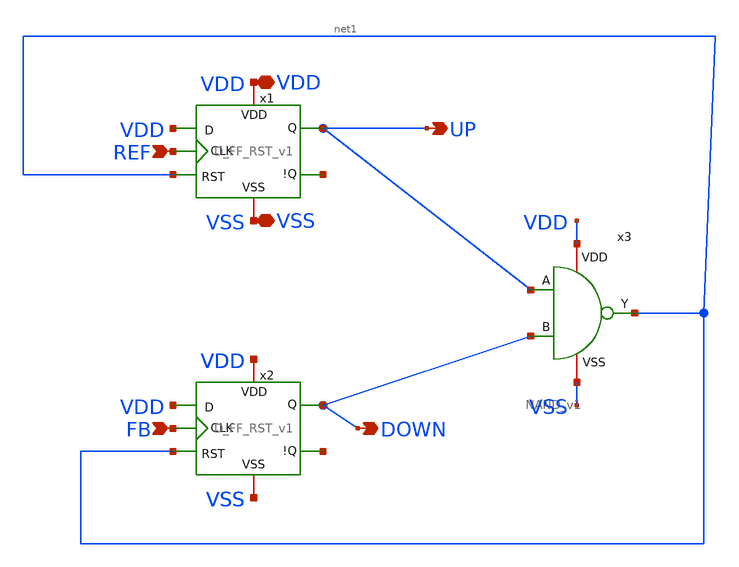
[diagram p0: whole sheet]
** sch_path: team_src/xschem/PFD_v1.sch
**.subckt PFD_v1 REF VSS VDD UP FB DOWN
*.ipin REF
*.iopin VSS
*.iopin VDD
*.opin UP
*.ipin FB
*.opin DOWN
x3 VDD net1 UP DOWN VSS NAND_v1
x1 net1 VDD VDD UP REF net2 VSS D_FF_RST_v1
x2 net1 VDD VDD DOWN FB net3 VSS D_FF_RST_v1
**.ends

* expanding   symbol:  NAND_v1.sym # of pins=5
** sym_path: team_src/xschem/NAND_v1.sym
** sch_path: team_src/xschem/NAND_v1.sch
.subckt NAND_v1 VDD Y A B VSS
*.iopin VSS
*.iopin VDD
*.ipin A
*.opin Y
*.ipin B
XM1 net1 B VSS VSS nfet_03v3 L=0.28u W=1u nf=1 ad='int((nf+1)/2) * W/nf * 0.18u' as='int((nf+2)/2) * W/nf * 0.18u'
+ pd='2*int((nf+1)/2) * (W/nf + 0.18u)' ps='2*int((nf+2)/2) * (W/nf + 0.18u)' nrd='0.18u / W' nrs='0.18u / W'
+ sa=0 sb=0 sd=0 m=1
XM2 Y A net1 VSS nfet_03v3 L=0.28u W=1u nf=1 ad='int((nf+1)/2) * W/nf * 0.18u' as='int((nf+2)/2) * W/nf * 0.18u'
+ pd='2*int((nf+1)/2) * (W/nf + 0.18u)' ps='2*int((nf+2)/2) * (W/nf + 0.18u)' nrd='0.18u / W' nrs='0.18u / W'
+ sa=0 sb=0 sd=0 m=1
XM3 Y B VDD VDD pfet_03v3 L=0.28u W=1u nf=1 ad='int((nf+1)/2) * W/nf * 0.18u' as='int((nf+2)/2) * W/nf * 0.18u'
+ pd='2*int((nf+1)/2) * (W/nf + 0.18u)' ps='2*int((nf+2)/2) * (W/nf + 0.18u)' nrd='0.18u / W' nrs='0.18u / W'
+ sa=0 sb=0 sd=0 m=1
XM4 Y A VDD VDD pfet_03v3 L=0.28u W=1u nf=1 ad='int((nf+1)/2) * W/nf * 0.18u' as='int((nf+2)/2) * W/nf * 0.18u'
+ pd='2*int((nf+1)/2) * (W/nf + 0.18u)' ps='2*int((nf+2)/2) * (W/nf + 0.18u)' nrd='0.18u / W' nrs='0.18u / W'
+ sa=0 sb=0 sd=0 m=1
.ends


* expanding   symbol:  D_FF_RST_v1.sym # of pins=7
** sym_path: team_src/xschem/D_FF_RST_v1.sym
** sch_path: team_src/xschem/D_FF_RST_v1.sch
.subckt D_FF_RST_v1 RST VDD D Q CLK !Q VSS
*.ipin CLK
*.ipin D
*.iopin VDD
*.opin Q
*.opin !Q
*.iopin VSS
*.ipin RST
x1 VDD Q net4 !Q VSS NAND_v1
x3 VDD net6 D net2 VSS NAND_v1
x4 VDD net5 net1 net2 VSS NAND_v1
x5 VDD D net1 VSS NOT_v1
x6 VDD net3 net2 VSS NOT_v1
x7 VDD CLK CLKB VSS NOT_v1
x8 VDD net3 CLK CLKB_DLY VSS NAND_v1
x2 RST VDD !Q Q net5 VSS NAND3_v1
x9 VDD net6 net7 VSS NOT_v1
x10 VDD net4 net7 RST VSS NAND_v1
x11 VDD CLKB net8 VSS NOT_v1
x12 VDD net12 CLKB_DLY VSS NOT_v1
x13 VDD net8 net9 VSS NOT_v1
x14 VDD net9 net10 VSS NOT_v1
x15 VDD net10 net11 VSS NOT_v1
x16 VDD net11 net12 VSS NOT_v1
.ends


* expanding   symbol:  NOT_v1.sym # of pins=4
** sym_path: team_src/xschem/NOT_v1.sym
** sch_path: team_src/xschem/NOT_v1.sch
.subckt NOT_v1 VDD A Y VSS
*.iopin VSS
*.iopin VDD
*.ipin A
*.opin Y
XM2 Y A VSS VSS nfet_03v3 L=0.28u W=1u nf=1 ad='int((nf+1)/2) * W/nf * 0.18u' as='int((nf+2)/2) * W/nf * 0.18u'
+ pd='2*int((nf+1)/2) * (W/nf + 0.18u)' ps='2*int((nf+2)/2) * (W/nf + 0.18u)' nrd='0.18u / W' nrs='0.18u / W'
+ sa=0 sb=0 sd=0 m=1
XM4 Y A VDD VDD pfet_03v3 L=0.28u W=1u nf=1 ad='int((nf+1)/2) * W/nf * 0.18u' as='int((nf+2)/2) * W/nf * 0.18u'
+ pd='2*int((nf+1)/2) * (W/nf + 0.18u)' ps='2*int((nf+2)/2) * (W/nf + 0.18u)' nrd='0.18u / W' nrs='0.18u / W'
+ sa=0 sb=0 sd=0 m=1
.ends


* expanding   symbol:  NAND3_v1.sym # of pins=6
** sym_path: team_src/xschem/NAND3_v1.sym
** sch_path: team_src/xschem/NAND3_v1.sch
.subckt NAND3_v1 C VDD Y A B VSS
*.iopin VSS
*.iopin VDD
*.ipin A
*.opin Y
*.ipin B
*.ipin C
XM1 net1 B net2 VSS nfet_03v3 L=0.28u W=3u nf=1 ad='int((nf+1)/2) * W/nf * 0.18u' as='int((nf+2)/2) * W/nf * 0.18u'
+ pd='2*int((nf+1)/2) * (W/nf + 0.18u)' ps='2*int((nf+2)/2) * (W/nf + 0.18u)' nrd='0.18u / W' nrs='0.18u / W'
+ sa=0 sb=0 sd=0 m=1
XM2 Y A net1 VSS nfet_03v3 L=0.28u W=3u nf=1 ad='int((nf+1)/2) * W/nf * 0.18u' as='int((nf+2)/2) * W/nf * 0.18u'
+ pd='2*int((nf+1)/2) * (W/nf + 0.18u)' ps='2*int((nf+2)/2) * (W/nf + 0.18u)' nrd='0.18u / W' nrs='0.18u / W'
+ sa=0 sb=0 sd=0 m=1
XM3 Y B VDD VDD pfet_03v3 L=0.28u W=1u nf=1 ad='int((nf+1)/2) * W/nf * 0.18u' as='int((nf+2)/2) * W/nf * 0.18u'
+ pd='2*int((nf+1)/2) * (W/nf + 0.18u)' ps='2*int((nf+2)/2) * (W/nf + 0.18u)' nrd='0.18u / W' nrs='0.18u / W'
+ sa=0 sb=0 sd=0 m=1
XM4 Y A VDD VDD pfet_03v3 L=0.28u W=1u nf=1 ad='int((nf+1)/2) * W/nf * 0.18u' as='int((nf+2)/2) * W/nf * 0.18u'
+ pd='2*int((nf+1)/2) * (W/nf + 0.18u)' ps='2*int((nf+2)/2) * (W/nf + 0.18u)' nrd='0.18u / W' nrs='0.18u / W'
+ sa=0 sb=0 sd=0 m=1
XM5 Y C VDD VDD pfet_03v3 L=0.28u W=1u nf=1 ad='int((nf+1)/2) * W/nf * 0.18u' as='int((nf+2)/2) * W/nf * 0.18u'
+ pd='2*int((nf+1)/2) * (W/nf + 0.18u)' ps='2*int((nf+2)/2) * (W/nf + 0.18u)' nrd='0.18u / W' nrs='0.18u / W'
+ sa=0 sb=0 sd=0 m=1
XM6 net2 C VSS VSS nfet_03v3 L=0.28u W=3u nf=1 ad='int((nf+1)/2) * W/nf * 0.18u' as='int((nf+2)/2) * W/nf * 0.18u'
+ pd='2*int((nf+1)/2) * (W/nf + 0.18u)' ps='2*int((nf+2)/2) * (W/nf + 0.18u)' nrd='0.18u / W' nrs='0.18u / W'
+ sa=0 sb=0 sd=0 m=1
.ends

.end
